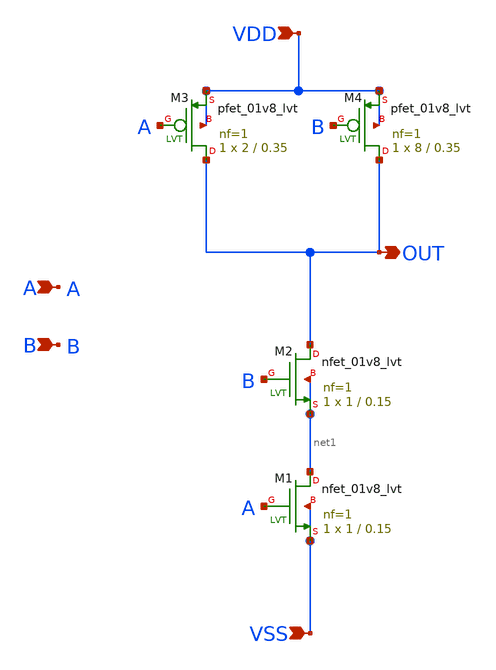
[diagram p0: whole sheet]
** sch_path: design/LELO_SVOD_SKY130A/LELO_NAND_OS_VC.sch
**.subckt LELO_NAND_OS_VC VDD VSS OUT A B
*.ipin VDD
*.ipin VSS
*.opin OUT
*.ipin A
*.ipin B
XM1 net1 A VSS VSS sky130_fd_pr__nfet_01v8_lvt L=0.15 W=1 nf=1 ad='int((1 + 1)/2) * 1 / 1 * 0.29' as='int((1 + 2)/2) * 1 / 1 * 0.29'
+ pd='2*int((1 + 1)/2) * (1 / 1 + 0.29)' ps='2*int((1 + 2)/2) * (1 / 1 + 0.29)' nrd='0.29 / 1 ' nrs='0.29 / 1 '
+ sa=0 sb=0 sd=0 mult=1 m=1
XM2 OUT B net1 net1 sky130_fd_pr__nfet_01v8_lvt L=0.15 W=1 nf=1 ad='int((1 + 1)/2) * 1 / 1 * 0.29' as='int((1 + 2)/2) * 1 / 1 * 0.29'
+ pd='2*int((1 + 1)/2) * (1 / 1 + 0.29)' ps='2*int((1 + 2)/2) * (1 / 1 + 0.29)' nrd='0.29 / 1 ' nrs='0.29 / 1 '
+ sa=0 sb=0 sd=0 mult=1 m=1
XM3 OUT A VDD VDD sky130_fd_pr__pfet_01v8_lvt L=0.35 W=2 nf=1 ad='int((1 + 1)/2) * 2 / 1 * 0.29' as='int((1 + 2)/2) * 2 / 1 * 0.29'
+ pd='2*int((1 + 1)/2) * (2 / 1 + 0.29)' ps='2*int((1 + 2)/2) * (2 / 1 + 0.29)' nrd='0.29 / 2 ' nrs='0.29 / 2 '
+ sa=0 sb=0 sd=0 mult=1 m=1
XM4 OUT B VDD VDD sky130_fd_pr__pfet_01v8_lvt L=0.35 W=8 nf=1 ad='int((1 + 1)/2) * 8 / 1 * 0.29' as='int((1 + 2)/2) * 8 / 1 * 0.29'
+ pd='2*int((1 + 1)/2) * (8 / 1 + 0.29)' ps='2*int((1 + 2)/2) * (8 / 1 + 0.29)' nrd='0.29 / 8 ' nrs='0.29 / 8 '
+ sa=0 sb=0 sd=0 mult=1 m=1
**.ends
.end
